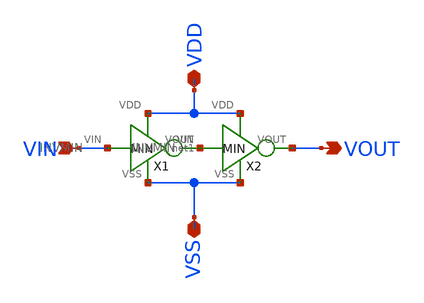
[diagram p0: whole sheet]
** sch_path: modules/BUFFMIN/symbol/BUFFMIN.sch
**.subckt BUFFMIN VDD VSS VIN VOUT
*.iopin VDD
*.iopin VSS
*.ipin VIN
*.opin VOUT
X1 VIN net1 VDD VSS INVMIN
X2 net1 VOUT VDD VSS INVMIN
**.ends
.end
